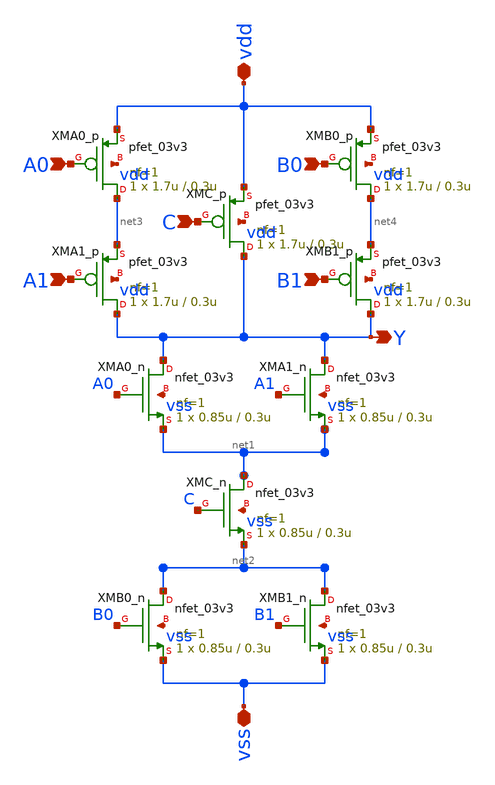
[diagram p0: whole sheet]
** sch_path: gf180mcu_osu_sc_gp9t3v3/xschem/gf180mcu_osu_sc_gp9t3v3__oai221_1.sch
**.subckt gf180mcu_osu_sc_gp9t3v3__oai221_1 A0 A1 C B0 B1 Y vss vdd
*.ipin A0
*.ipin A1
*.ipin C
*.ipin B0
*.ipin B1
*.opin Y
*.iopin vss
*.iopin vdd
XMB0_n net2 B0 vss vss nfet_03v3 L=0.3u W=0.85u nf=1 ad='int((nf+1)/2) * W/nf * 0.18u' as='int((nf+2)/2) * W/nf * 0.18u'
+ pd='2*int((nf+1)/2) * (W/nf + 0.18u)' ps='2*int((nf+2)/2) * (W/nf + 0.18u)' nrd='0.18u / W' nrs='0.18u / W'
+ sa=0 sb=0 sd=0 m=1
XMC_p Y C vdd vdd pfet_03v3 L=0.3u W=1.7u nf=1 ad='int((nf+1)/2) * W/nf * 0.18u' as='int((nf+2)/2) * W/nf * 0.18u'
+ pd='2*int((nf+1)/2) * (W/nf + 0.18u)' ps='2*int((nf+2)/2) * (W/nf + 0.18u)' nrd='0.18u / W' nrs='0.18u / W'
+ sa=0 sb=0 sd=0 m=1
XMB1_n net2 B1 vss vss nfet_03v3 L=0.3u W=0.85u nf=1 ad='int((nf+1)/2) * W/nf * 0.18u' as='int((nf+2)/2) * W/nf * 0.18u'
+ pd='2*int((nf+1)/2) * (W/nf + 0.18u)' ps='2*int((nf+2)/2) * (W/nf + 0.18u)' nrd='0.18u / W' nrs='0.18u / W'
+ sa=0 sb=0 sd=0 m=1
XMC_n net1 C net2 vss nfet_03v3 L=0.3u W=0.85u nf=1 ad='int((nf+1)/2) * W/nf * 0.18u' as='int((nf+2)/2) * W/nf * 0.18u'
+ pd='2*int((nf+1)/2) * (W/nf + 0.18u)' ps='2*int((nf+2)/2) * (W/nf + 0.18u)' nrd='0.18u / W' nrs='0.18u / W'
+ sa=0 sb=0 sd=0 m=1
XMA0_n Y A0 net1 vss nfet_03v3 L=0.3u W=0.85u nf=1 ad='int((nf+1)/2) * W/nf * 0.18u' as='int((nf+2)/2) * W/nf * 0.18u'
+ pd='2*int((nf+1)/2) * (W/nf + 0.18u)' ps='2*int((nf+2)/2) * (W/nf + 0.18u)' nrd='0.18u / W' nrs='0.18u / W'
+ sa=0 sb=0 sd=0 m=1
XMA1_n Y A1 net1 vss nfet_03v3 L=0.3u W=0.85u nf=1 ad='int((nf+1)/2) * W/nf * 0.18u' as='int((nf+2)/2) * W/nf * 0.18u'
+ pd='2*int((nf+1)/2) * (W/nf + 0.18u)' ps='2*int((nf+2)/2) * (W/nf + 0.18u)' nrd='0.18u / W' nrs='0.18u / W'
+ sa=0 sb=0 sd=0 m=1
XMA1_p Y A1 net3 vdd pfet_03v3 L=0.3u W=1.7u nf=1 ad='int((nf+1)/2) * W/nf * 0.18u' as='int((nf+2)/2) * W/nf * 0.18u'
+ pd='2*int((nf+1)/2) * (W/nf + 0.18u)' ps='2*int((nf+2)/2) * (W/nf + 0.18u)' nrd='0.18u / W' nrs='0.18u / W'
+ sa=0 sb=0 sd=0 m=1
XMB1_p Y B1 net4 vdd pfet_03v3 L=0.3u W=1.7u nf=1 ad='int((nf+1)/2) * W/nf * 0.18u' as='int((nf+2)/2) * W/nf * 0.18u'
+ pd='2*int((nf+1)/2) * (W/nf + 0.18u)' ps='2*int((nf+2)/2) * (W/nf + 0.18u)' nrd='0.18u / W' nrs='0.18u / W'
+ sa=0 sb=0 sd=0 m=1
XMA0_p net3 A0 vdd vdd pfet_03v3 L=0.3u W=1.7u nf=1 ad='int((nf+1)/2) * W/nf * 0.18u' as='int((nf+2)/2) * W/nf * 0.18u'
+ pd='2*int((nf+1)/2) * (W/nf + 0.18u)' ps='2*int((nf+2)/2) * (W/nf + 0.18u)' nrd='0.18u / W' nrs='0.18u / W'
+ sa=0 sb=0 sd=0 m=1
XMB0_p net4 B0 vdd vdd pfet_03v3 L=0.3u W=1.7u nf=1 ad='int((nf+1)/2) * W/nf * 0.18u' as='int((nf+2)/2) * W/nf * 0.18u'
+ pd='2*int((nf+1)/2) * (W/nf + 0.18u)' ps='2*int((nf+2)/2) * (W/nf + 0.18u)' nrd='0.18u / W' nrs='0.18u / W'
+ sa=0 sb=0 sd=0 m=1
**.ends
.end
